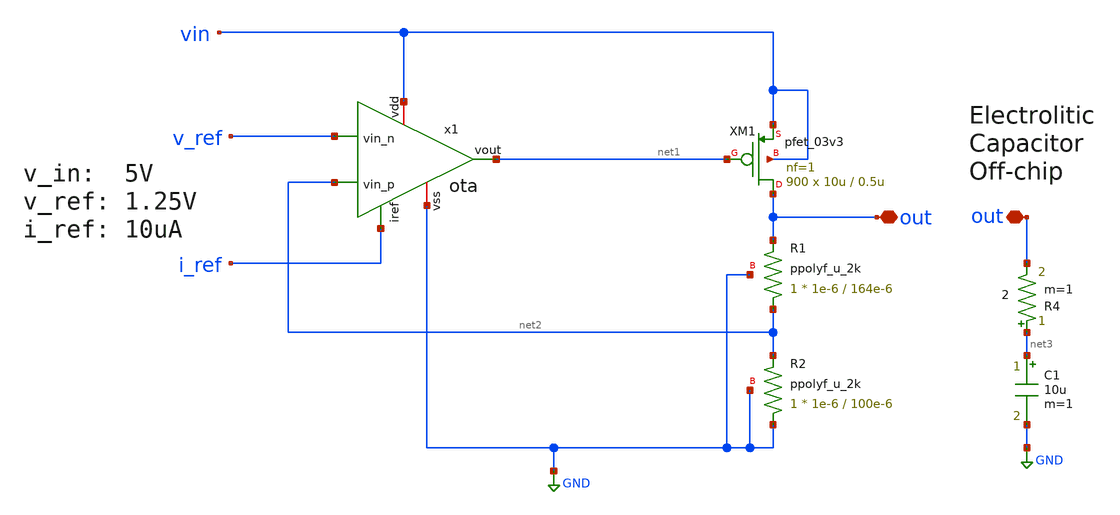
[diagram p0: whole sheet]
** sch_path: LDO/xschem/ldo/test/diagram.sch
**.subckt diagram out out
*.iopin out
*.iopin out
XM1 out net1 vin vin pfet_03v3 L=0.5u W=10u nf=1 ad='int((nf+1)/2) * W/nf * 0.18u' as='int((nf+2)/2) * W/nf * 0.18u'
+ pd='2*int((nf+1)/2) * (W/nf + 0.18u)' ps='2*int((nf+2)/2) * (W/nf + 0.18u)' nrd='0.18u / W' nrs='0.18u / W'
+ sa=0 sb=0 sd=0 m=900
XR1 net2 out GND ppolyf_u_2k r_width=1e-6 r_length=164e-6 m=1
XR2 GND net2 GND ppolyf_u_2k r_width=1e-6 r_length=100e-6 m=1
x1 vin i_ref v_ref net2 net1 GND ota
C1 net3 GND 10u m=1
R4 net3 out 2 m=1
**.ends
.GLOBAL GND
.end
